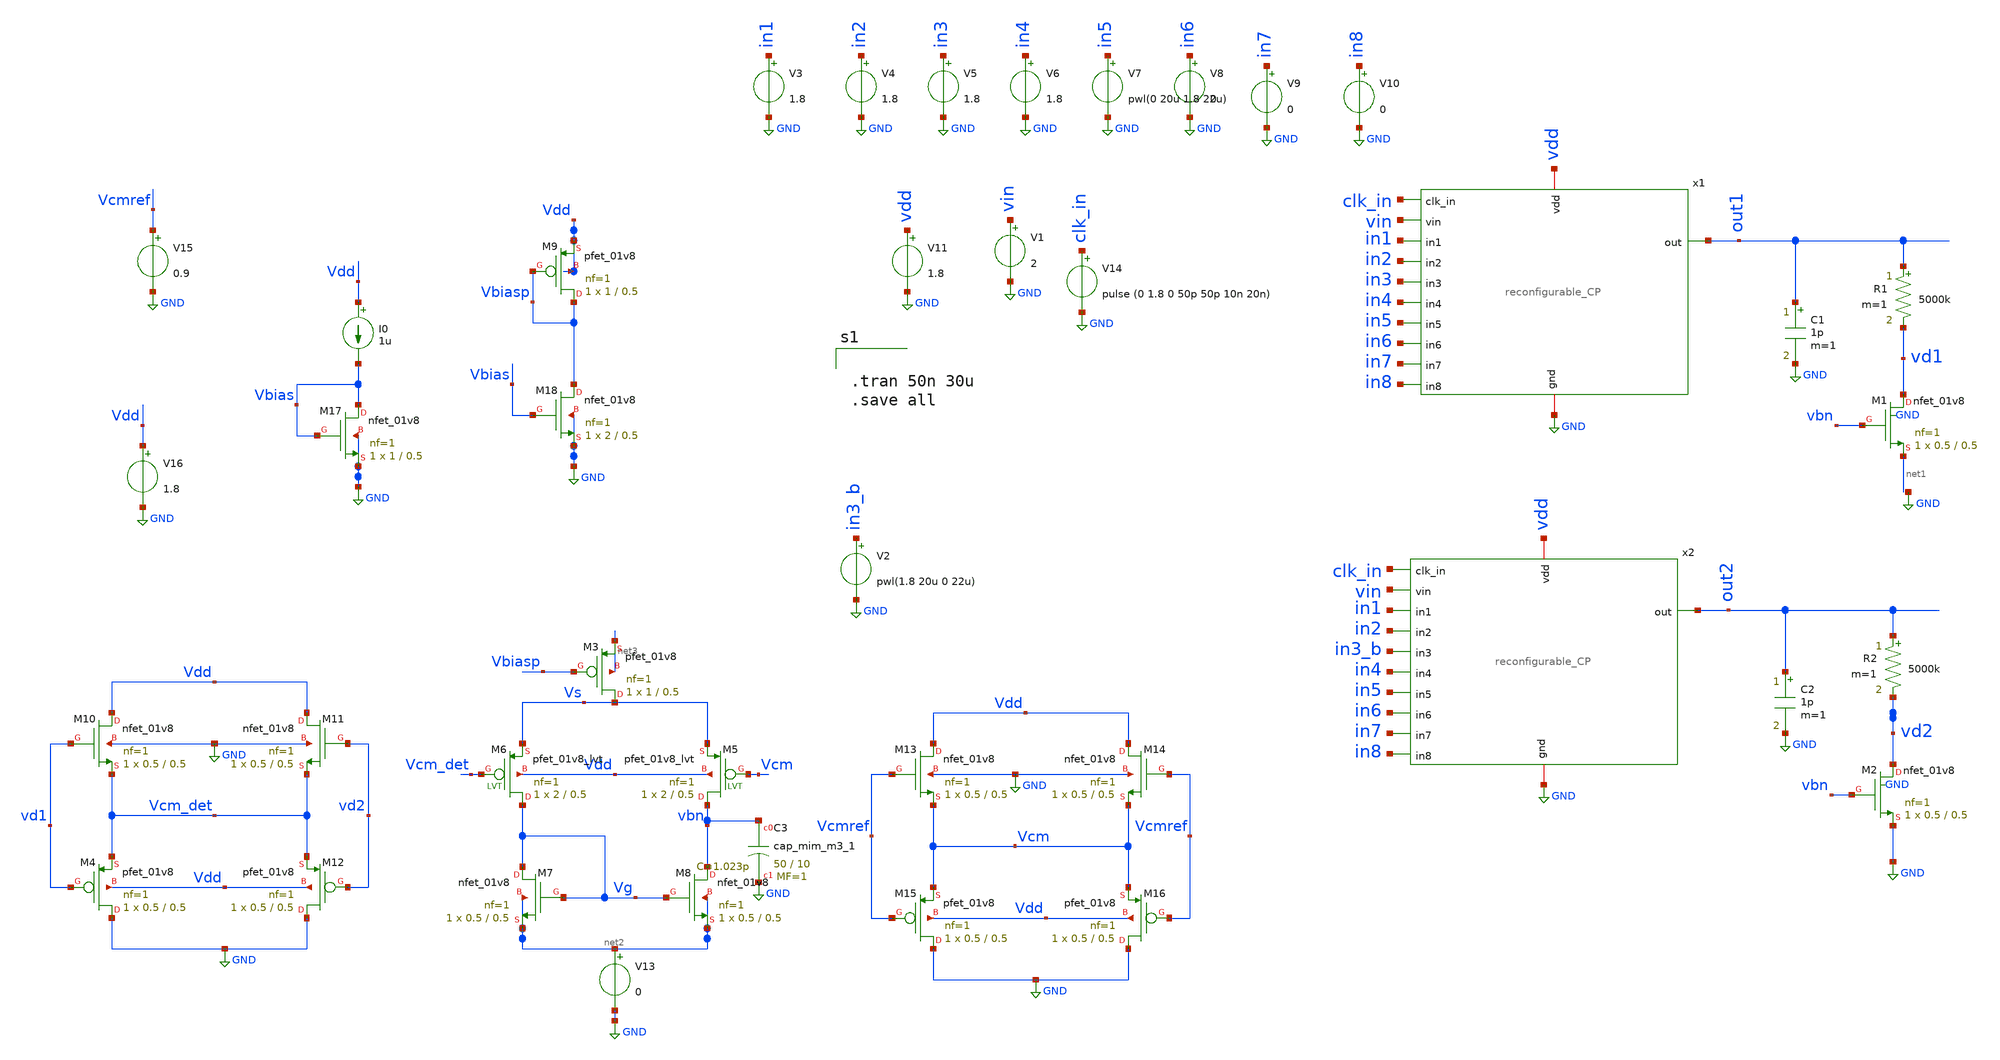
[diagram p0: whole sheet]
** sch_path: xschem/charge_pumps2/CP_withCMFB2.sch
**.subckt CP_withCMFB2
x1 clk_in vin out1 in1 in2 in3 in4 in5 in6 in7 in8 vdd GND reconfigurable_CP
V3 in1 GND 1.8
V4 in2 GND 1.8
V5 in3 GND 1.8
V6 in4 GND 1.8
V8 in6 GND 0
V9 in7 GND 0
V10 in8 GND 0
V1 vin GND 2
V11 vdd GND 1.8
V14 clk_in GND pulse (0 1.8 0 50p 50p 10n 20n)
C1 out1 GND 1p m=1
R1 out1 vd1 5000k m=1
XM1 vd1 vbn net1 GND sky130_fd_pr__nfet_01v8 L=0.5 W=0.5 nf=1 ad='int((nf+1)/2) * W/nf * 0.29' as='int((nf+2)/2) * W/nf * 0.29'
+ pd='2*int((nf+1)/2) * (W/nf + 0.29)' ps='2*int((nf+2)/2) * (W/nf + 0.29)' nrd='0.29 / W' nrs='0.29 / W'
+ sa=0 sb=0 sd=0 mult=1 m=1
x2 clk_in vin out2 in1 in2 in3_b in4 in5 in6 in7 in8 vdd GND reconfigurable_CP
C2 out2 GND 1p m=1
R2 out2 vd2 5000k m=1
XM2 vd2 vbn GND GND sky130_fd_pr__nfet_01v8 L=0.5 W=0.5 nf=1 ad='int((nf+1)/2) * W/nf * 0.29' as='int((nf+2)/2) * W/nf * 0.29'
+ pd='2*int((nf+1)/2) * (W/nf + 0.29)' ps='2*int((nf+2)/2) * (W/nf + 0.29)' nrd='0.29 / W' nrs='0.29 / W'
+ sa=0 sb=0 sd=0 mult=1 m=1
V2 in3_b GND pwl(1.8 20u 0 22u)
XM4 GND vd1 Vcm_det Vdd sky130_fd_pr__pfet_01v8 L=0.5 W=0.5 nf=1 ad='int((nf+1)/2) * W/nf * 0.29' as='int((nf+2)/2) * W/nf * 0.29'
+ pd='2*int((nf+1)/2) * (W/nf + 0.29)' ps='2*int((nf+2)/2) * (W/nf + 0.29)' nrd='0.29 / W' nrs='0.29 / W'
+ sa=0 sb=0 sd=0 mult=1 m=1
XM12 GND vd2 Vcm_det Vdd sky130_fd_pr__pfet_01v8 L=0.5 W=0.5 nf=1 ad='int((nf+1)/2) * W/nf * 0.29' as='int((nf+2)/2) * W/nf * 0.29'
+ pd='2*int((nf+1)/2) * (W/nf + 0.29)' ps='2*int((nf+2)/2) * (W/nf + 0.29)' nrd='0.29 / W' nrs='0.29 / W'
+ sa=0 sb=0 sd=0 mult=1 m=1
XM10 Vdd vd1 Vcm_det GND sky130_fd_pr__nfet_01v8 L=0.5 W=0.5 nf=1 ad='int((nf+1)/2) * W/nf * 0.29' as='int((nf+2)/2) * W/nf * 0.29'
+ pd='2*int((nf+1)/2) * (W/nf + 0.29)' ps='2*int((nf+2)/2) * (W/nf + 0.29)' nrd='0.29 / W' nrs='0.29 / W'
+ sa=0 sb=0 sd=0 mult=1 m=1
XM11 Vdd vd2 Vcm_det GND sky130_fd_pr__nfet_01v8 L=0.5 W=0.5 nf=1 ad='int((nf+1)/2) * W/nf * 0.29' as='int((nf+2)/2) * W/nf * 0.29'
+ pd='2*int((nf+1)/2) * (W/nf + 0.29)' ps='2*int((nf+2)/2) * (W/nf + 0.29)' nrd='0.29 / W' nrs='0.29 / W'
+ sa=0 sb=0 sd=0 mult=1 m=1
XM7 Vg Vg net2 net2 sky130_fd_pr__nfet_01v8 L=0.5 W=0.5 nf=1 ad='int((nf+1)/2) * W/nf * 0.29' as='int((nf+2)/2) * W/nf * 0.29'
+ pd='2*int((nf+1)/2) * (W/nf + 0.29)' ps='2*int((nf+2)/2) * (W/nf + 0.29)' nrd='0.29 / W' nrs='0.29 / W'
+ sa=0 sb=0 sd=0 mult=1 m=1
XM8 vbn Vg net2 net2 sky130_fd_pr__nfet_01v8 L=0.5 W=0.5 nf=1 ad='int((nf+1)/2) * W/nf * 0.29' as='int((nf+2)/2) * W/nf * 0.29'
+ pd='2*int((nf+1)/2) * (W/nf + 0.29)' ps='2*int((nf+2)/2) * (W/nf + 0.29)' nrd='0.29 / W' nrs='0.29 / W'
+ sa=0 sb=0 sd=0 mult=1 m=1
XM13 Vdd Vcmref Vcm GND sky130_fd_pr__nfet_01v8 L=0.5 W=0.5 nf=1 ad='int((nf+1)/2) * W/nf * 0.29' as='int((nf+2)/2) * W/nf * 0.29'
+ pd='2*int((nf+1)/2) * (W/nf + 0.29)' ps='2*int((nf+2)/2) * (W/nf + 0.29)' nrd='0.29 / W' nrs='0.29 / W'
+ sa=0 sb=0 sd=0 mult=1 m=1
XM14 Vdd Vcmref Vcm GND sky130_fd_pr__nfet_01v8 L=0.5 W=0.5 nf=1 ad='int((nf+1)/2) * W/nf * 0.29' as='int((nf+2)/2) * W/nf * 0.29'
+ pd='2*int((nf+1)/2) * (W/nf + 0.29)' ps='2*int((nf+2)/2) * (W/nf + 0.29)' nrd='0.29 / W' nrs='0.29 / W'
+ sa=0 sb=0 sd=0 mult=1 m=1
XM15 GND Vcmref Vcm Vdd sky130_fd_pr__pfet_01v8 L=0.5 W=0.5 nf=1 ad='int((nf+1)/2) * W/nf * 0.29' as='int((nf+2)/2) * W/nf * 0.29'
+ pd='2*int((nf+1)/2) * (W/nf + 0.29)' ps='2*int((nf+2)/2) * (W/nf + 0.29)' nrd='0.29 / W' nrs='0.29 / W'
+ sa=0 sb=0 sd=0 mult=1 m=1
XM16 GND Vcmref Vcm Vdd sky130_fd_pr__pfet_01v8 L=0.5 W=0.5 nf=1 ad='int((nf+1)/2) * W/nf * 0.29' as='int((nf+2)/2) * W/nf * 0.29'
+ pd='2*int((nf+1)/2) * (W/nf + 0.29)' ps='2*int((nf+2)/2) * (W/nf + 0.29)' nrd='0.29 / W' nrs='0.29 / W'
+ sa=0 sb=0 sd=0 mult=1 m=1
XM3 Vs Vbiasp net3 net3 sky130_fd_pr__pfet_01v8 L=0.5 W=1 nf=1 ad='int((nf+1)/2) * W/nf * 0.29' as='int((nf+2)/2) * W/nf * 0.29'
+ pd='2*int((nf+1)/2) * (W/nf + 0.29)' ps='2*int((nf+2)/2) * (W/nf + 0.29)' nrd='0.29 / W' nrs='0.29 / W'
+ sa=0 sb=0 sd=0 mult=1 m=1
V13 net2 GND 0
XM5 vbn Vcm Vs Vdd sky130_fd_pr__pfet_01v8_lvt L=0.5 W=2 nf=1 ad='int((nf+1)/2) * W/nf * 0.29' as='int((nf+2)/2) * W/nf * 0.29'
+ pd='2*int((nf+1)/2) * (W/nf + 0.29)' ps='2*int((nf+2)/2) * (W/nf + 0.29)' nrd='0.29 / W' nrs='0.29 / W'
+ sa=0 sb=0 sd=0 mult=1 m=1
XM6 Vg Vcm_det Vs Vdd sky130_fd_pr__pfet_01v8_lvt L=0.5 W=2 nf=1 ad='int((nf+1)/2) * W/nf * 0.29' as='int((nf+2)/2) * W/nf * 0.29'
+ pd='2*int((nf+1)/2) * (W/nf + 0.29)' ps='2*int((nf+2)/2) * (W/nf + 0.29)' nrd='0.29 / W' nrs='0.29 / W'
+ sa=0 sb=0 sd=0 mult=1 m=1
V15 Vcmref GND 0.9
XM9 Vbiasp Vbiasp Vdd Vdd sky130_fd_pr__pfet_01v8 L=0.5 W=1 nf=1 ad='int((nf+1)/2) * W/nf * 0.29' as='int((nf+2)/2) * W/nf * 0.29'
+ pd='2*int((nf+1)/2) * (W/nf + 0.29)' ps='2*int((nf+2)/2) * (W/nf + 0.29)' nrd='0.29 / W' nrs='0.29 / W'
+ sa=0 sb=0 sd=0 mult=1 m=1
I0 Vdd Vbias 1u
XM17 Vbias Vbias GND GND sky130_fd_pr__nfet_01v8 L=0.5 W=1 nf=1 ad='int((nf+1)/2) * W/nf * 0.29' as='int((nf+2)/2) * W/nf * 0.29'
+ pd='2*int((nf+1)/2) * (W/nf + 0.29)' ps='2*int((nf+2)/2) * (W/nf + 0.29)' nrd='0.29 / W' nrs='0.29 / W'
+ sa=0 sb=0 sd=0 mult=1 m=1
XM18 Vbiasp Vbias GND GND sky130_fd_pr__nfet_01v8 L=0.5 W=2 nf=1 ad='int((nf+1)/2) * W/nf * 0.29' as='int((nf+2)/2) * W/nf * 0.29'
+ pd='2*int((nf+1)/2) * (W/nf + 0.29)' ps='2*int((nf+2)/2) * (W/nf + 0.29)' nrd='0.29 / W' nrs='0.29 / W'
+ sa=0 sb=0 sd=0 mult=1 m=1
V16 Vdd GND 1.8
V7 in5 GND pwl(0 20u 1.8 22u)
XC3 vbn GND sky130_fd_pr__cap_mim_m3_1 W=50 L=10 MF=1 m=1
**** begin user architecture code


.tran 50n 30u
.save all



** opencircuitdesign pdks install
.lib $::SKYWATER_MODELS/sky130.lib.spice tt


**** end user architecture code
**.ends
.GLOBAL GND
.end
